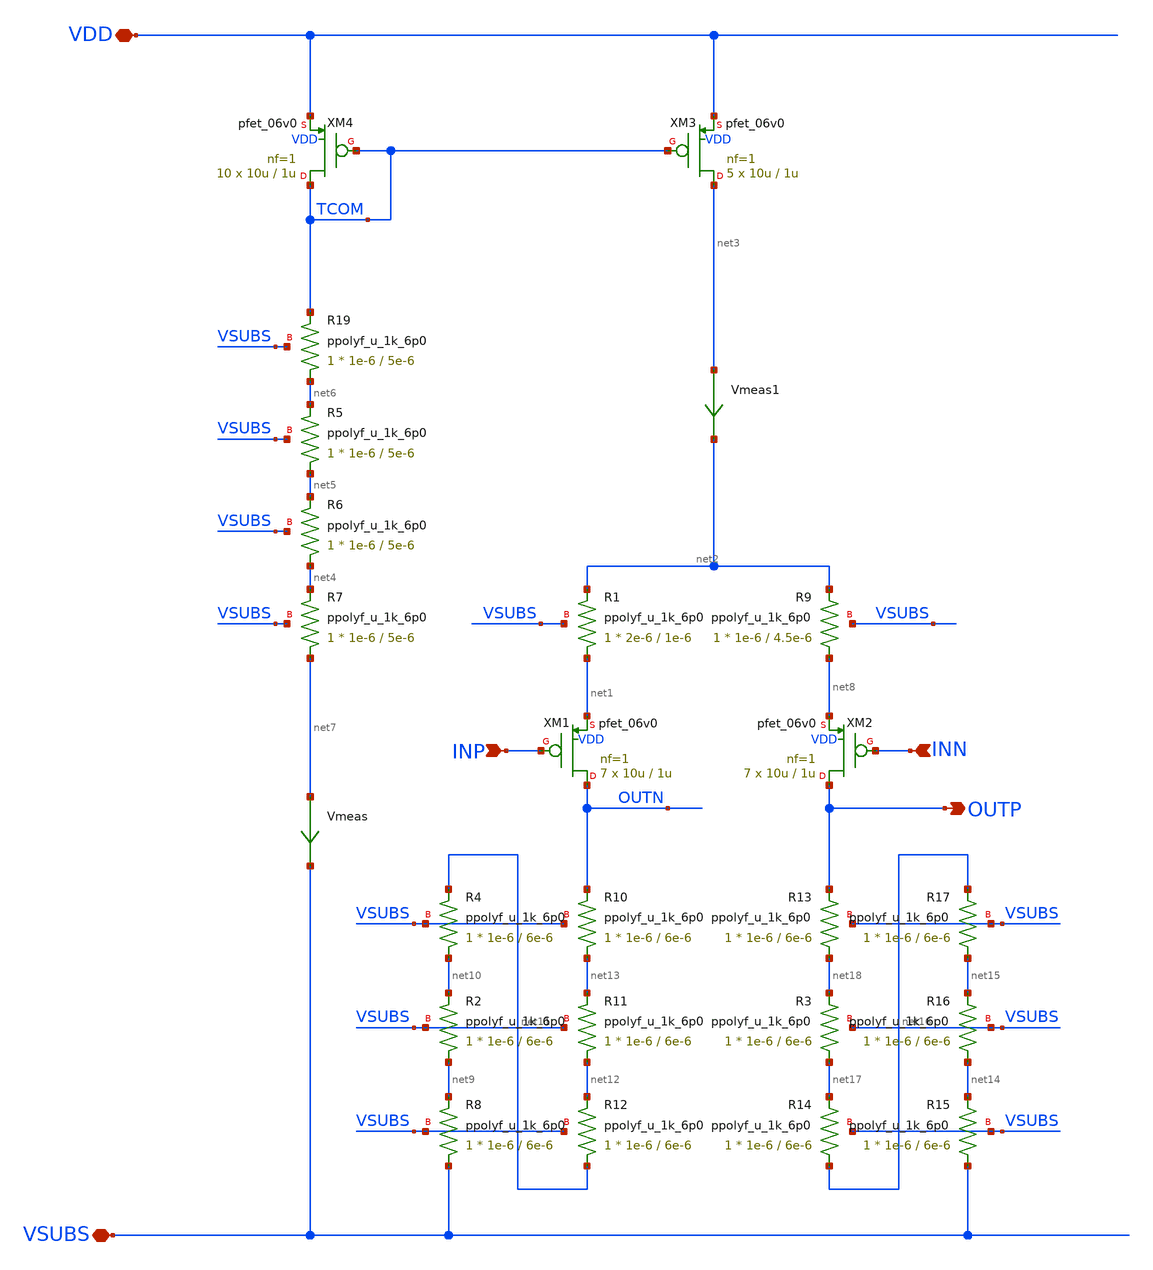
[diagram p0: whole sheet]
** sch_path: xschem/ip_amplifier.sch
**.subckt ip_amplifier VDD VSUBS INP INN OUTP
*.iopin VDD
*.iopin VSUBS
*.ipin INP
*.ipin INN
*.opin OUTP
Vmeas net7 VSUBS 0
Vmeas1 net3 net2 0
XM4 TCOM TCOM VDD VDD pfet_06v0 L=1u W=10u nf=1 ad='int((nf+1)/2) * W/nf * 0.18u' as='int((nf+2)/2) * W/nf * 0.18u'
+ pd='2*int((nf+1)/2) * (W/nf + 0.18u)' ps='2*int((nf+2)/2) * (W/nf + 0.18u)' nrd='0.18u / W' nrs='0.18u / W'
+ sa=0 sb=0 sd=0 m=10 par=10
XM3 net3 TCOM VDD VDD pfet_06v0 L=1u W=10u nf=1 ad='int((nf+1)/2) * W/nf * 0.18u' as='int((nf+2)/2) * W/nf * 0.18u'
+ pd='2*int((nf+1)/2) * (W/nf + 0.18u)' ps='2*int((nf+2)/2) * (W/nf + 0.18u)' nrd='0.18u / W' nrs='0.18u / W'
+ sa=0 sb=0 sd=0 m=5 par=5
XM1 OUTN INP net1 VDD pfet_06v0 L=1u W=10u nf=1 ad='int((nf+1)/2) * W/nf * 0.18u' as='int((nf+2)/2) * W/nf * 0.18u'
+ pd='2*int((nf+1)/2) * (W/nf + 0.18u)' ps='2*int((nf+2)/2) * (W/nf + 0.18u)' nrd='0.18u / W' nrs='0.18u / W'
+ sa=0 sb=0 sd=0 m=7 par=7
XM2 OUTP INN net8 VDD pfet_06v0 L=1u W=10u nf=1 ad='int((nf+1)/2) * W/nf * 0.18u' as='int((nf+2)/2) * W/nf * 0.18u'
+ pd='2*int((nf+1)/2) * (W/nf + 0.18u)' ps='2*int((nf+2)/2) * (W/nf + 0.18u)' nrd='0.18u / W' nrs='0.18u / W'
+ sa=0 sb=0 sd=0 m=7 par=7
XR19 net6 TCOM VSUBS ppolyf_u_1k_6p0 r_width=1e-6 r_length=5e-6 m=1
XR5 net5 net6 VSUBS ppolyf_u_1k_6p0 r_width=1e-6 r_length=5e-6 m=1
XR4 net10 net11 VSUBS ppolyf_u_1k_6p0 r_width=1e-6 r_length=6e-6 m=1
XR2 net9 net10 VSUBS ppolyf_u_1k_6p0 r_width=1e-6 r_length=6e-6 m=1
XR8 VSUBS net9 VSUBS ppolyf_u_1k_6p0 r_width=1e-6 r_length=6e-6 m=1
XR12 net11 net12 VSUBS ppolyf_u_1k_6p0 r_width=1e-6 r_length=6e-6 m=1
XR11 net12 net13 VSUBS ppolyf_u_1k_6p0 r_width=1e-6 r_length=6e-6 m=1
XR10 net13 OUTN VSUBS ppolyf_u_1k_6p0 r_width=1e-6 r_length=6e-6 m=1
XR13 net18 OUTP VSUBS ppolyf_u_1k_6p0 r_width=1e-6 r_length=6e-6 m=1
XR3 net17 net18 VSUBS ppolyf_u_1k_6p0 r_width=1e-6 r_length=6e-6 m=1
XR14 net16 net17 VSUBS ppolyf_u_1k_6p0 r_width=1e-6 r_length=6e-6 m=1
XR15 VSUBS net14 VSUBS ppolyf_u_1k_6p0 r_width=1e-6 r_length=6e-6 m=1
XR16 net14 net15 VSUBS ppolyf_u_1k_6p0 r_width=1e-6 r_length=6e-6 m=1
XR17 net15 net16 VSUBS ppolyf_u_1k_6p0 r_width=1e-6 r_length=6e-6 m=1
XR9 net8 net2 VSUBS ppolyf_u_1k_6p0 r_width=1e-6 r_length=4.5e-6 m=1
XR1 net1 net2 VSUBS ppolyf_u_1k_6p0 r_width=2e-6 r_length=1e-6 m=1
XR6 net4 net5 VSUBS ppolyf_u_1k_6p0 r_width=1e-6 r_length=5e-6 m=1
XR7 net7 net4 VSUBS ppolyf_u_1k_6p0 r_width=1e-6 r_length=5e-6 m=1
**.ends
.end
